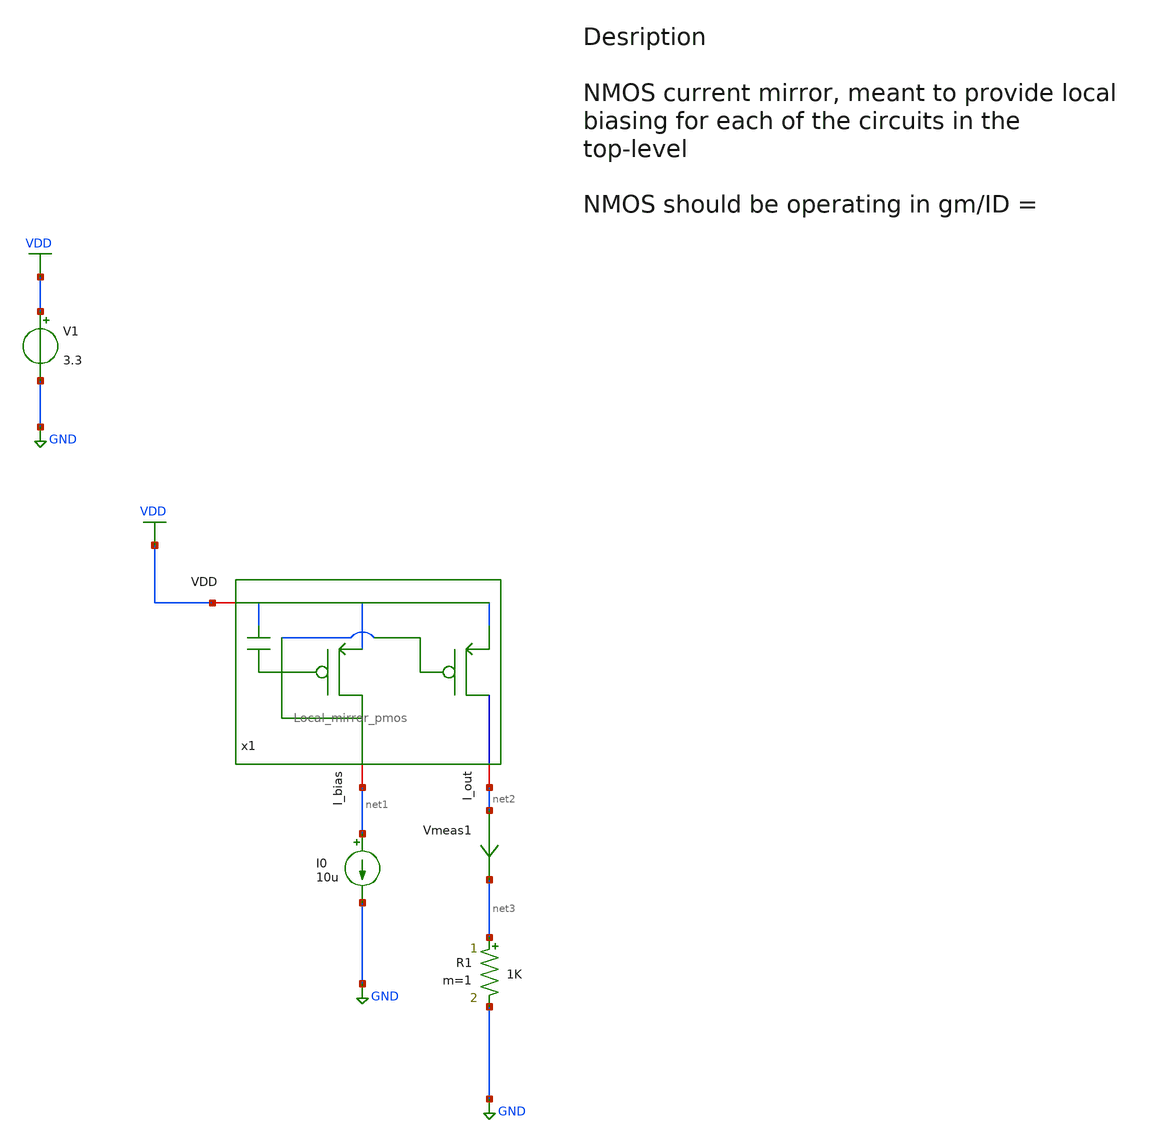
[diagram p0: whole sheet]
** sch_path: src/design_tb/Local_mirror_pmos_tb.sch
**.subckt Local_mirror_pmos_tb
I0 net1 GND 10u
V1 VDD GND 3.3
.save i(v1)
Vmeas1 net2 net3 0
.save i(vmeas1)
R1 net3 GND 1K m=1
x1 VDD net2 net1 Local_mirror_pmos w_ref=2u l_ref=0.4u w_mir=6u l_mir=0.4u
**** begin user architecture code

.include $::180MCU_MODELS/design.ngspice
.lib $::180MCU_MODELS/sm141064.ngspice typical
.lib $::180MCU_MODELS/sm141064.ngspice mimcap_typical
.lib $::180MCU_MODELS/sm141064.ngspice cap_mim
.lib $::180MCU_MODELS/sm141064.ngspice res_typical
.lib $::180MCU_MODELS/sm141064.ngspice diode_typical



* Add convergence aids
.option method=gear

.control

    * operating point
    op
    show

    write Local_mirror_pmos_tb.raw

    set appendwrite

    * Transient analysis to observe mixing operation
    tran 1n 0.01u
    write Local_mirror_pmos_tb.raw

.endc


**** end user architecture code
**.ends
.GLOBAL GND
.GLOBAL VDD
.end
